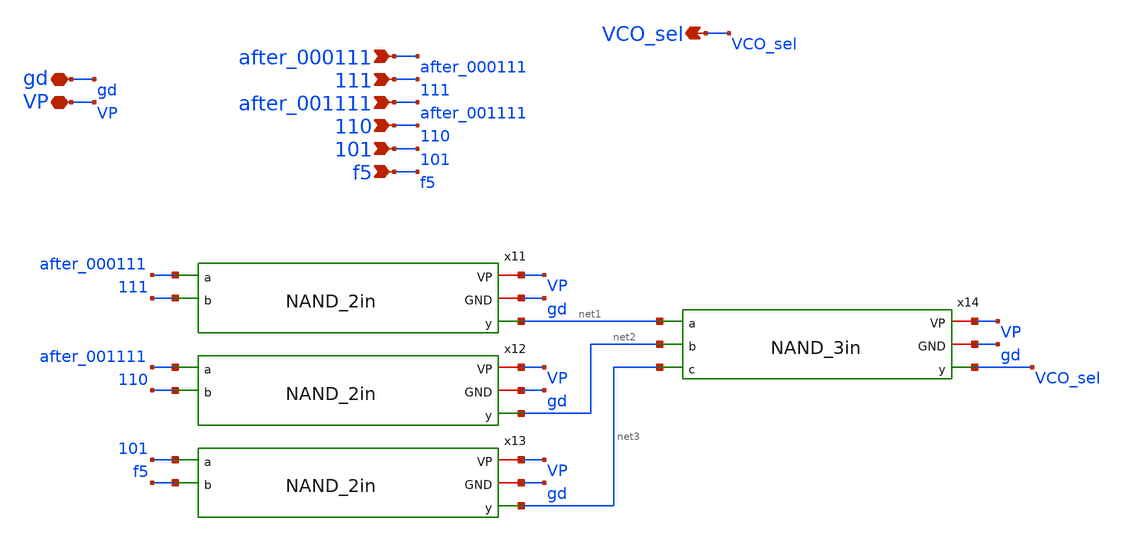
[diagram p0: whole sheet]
** sch_path: schematics/divider/schematics/VCO_selection.sch
**.subckt VCO_selection gd VP after_000111 111 after_001111 110 101 f5 VCO_sel
*.iopin gd
*.iopin VP
*.ipin after_000111
*.ipin 111
*.ipin after_001111
*.ipin 110
*.ipin 101
*.ipin f5
*.opin VCO_sel
x11 VP gd after_000111 net1 111 NAND_2in
x12 VP gd after_001111 net2 110 NAND_2in
x13 VP gd 101 net3 f5 NAND_2in
x14 VP gd net1 VCO_sel net2 net3 NAND_3in
**.ends

* expanding   symbol:  NAND_2in.sym # of pins=5
** sym_path: schematics/divider/schematics/NAND_2in.sym
** sch_path: schematics/divider/schematics/NAND_2in.sch
.subckt NAND_2in VP GND a y b
*.opin y
*.iopin GND
*.ipin a
*.iopin VP
*.ipin b
XM1 y a net1 GND sg13_lv_nmos w=0.15u l=0.13u ng=1 m=1 mm_ok=1
XM3 net1 b GND GND sg13_lv_nmos w=0.15u l=0.13u ng=1 m=1 mm_ok=1
XM2 y b VP VP sg13_lv_pmos w=0.15u l=0.13u ng=1 m=1 mm_ok=1
XM4 y a VP VP sg13_lv_pmos w=0.15u l=0.13u ng=1 m=1 mm_ok=1
.ends


* expanding   symbol:  NAND_3in.sym # of pins=6
** sym_path: schematics/divider/schematics/NAND_3in.sym
** sch_path: schematics/divider/schematics/NAND_3in.sch
.subckt NAND_3in VP GND a y b c
*.opin y
*.iopin GND
*.ipin a
*.iopin VP
*.ipin b
*.ipin c
XM1 y a net2 GND sg13_lv_nmos w=0.15u l=0.13u ng=1 m=1 mm_ok=1
XM3 net2 b net1 GND sg13_lv_nmos w=0.15u l=0.13u ng=1 m=1 mm_ok=1
XM4 net1 c GND GND sg13_lv_nmos w=0.15u l=0.13u ng=1 m=1 mm_ok=1
XM7 y c VP VP sg13_lv_pmos w=0.15u l=0.13u ng=1 m=1 mm_ok=1
XM2 y a VP VP sg13_lv_pmos w=0.15u l=0.13u ng=1 m=1 mm_ok=1
XM5 y b VP VP sg13_lv_pmos w=0.15u l=0.13u ng=1 m=1 mm_ok=1
.ends

.end
